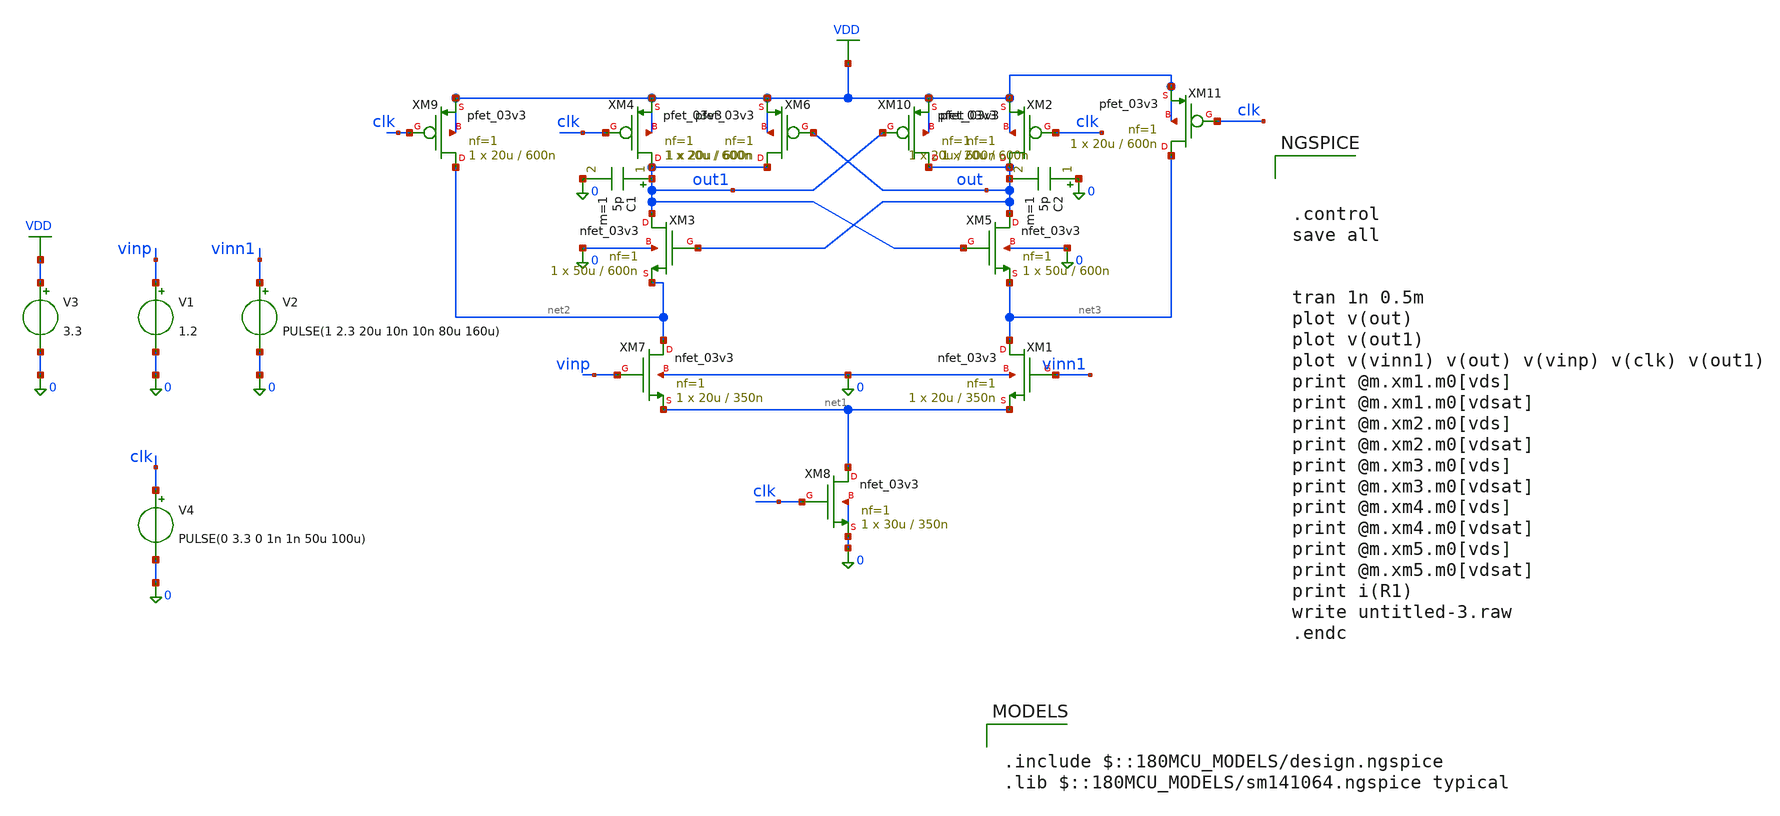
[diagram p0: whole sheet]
** sch_path: amplifier/untitled-3.sch
**.subckt untitled-3
XM4 out1 clk VDD VDD pfet_03v3 L=600n W=20u nf=1 ad='int((nf+1)/2) * W/nf * 0.18u' as='int((nf+2)/2) * W/nf * 0.18u'
+ pd='2*int((nf+1)/2) * (W/nf + 0.18u)' ps='2*int((nf+2)/2) * (W/nf + 0.18u)' nrd='0.18u / W' nrs='0.18u / W'
+ sa=0 sb=0 sd=0 m=1
V1 vinp 0 1.2
V2 vinn1 0 PULSE(1 2.3 20u 10n 10n 80u 160u)
V3 VDD 0 3.3
XM2 out clk VDD VDD pfet_03v3 L=600n W=20u nf=1 ad='int((nf+1)/2) * W/nf * 0.18u' as='int((nf+2)/2) * W/nf * 0.18u'
+ pd='2*int((nf+1)/2) * (W/nf + 0.18u)' ps='2*int((nf+2)/2) * (W/nf + 0.18u)' nrd='0.18u / W' nrs='0.18u / W'
+ sa=0 sb=0 sd=0 m=1
XM7 net2 vinp net1 0 nfet_03v3 L=350n W=20u nf=1 ad='int((nf+1)/2) * W/nf * 0.18u' as='int((nf+2)/2) * W/nf * 0.18u'
+ pd='2*int((nf+1)/2) * (W/nf + 0.18u)' ps='2*int((nf+2)/2) * (W/nf + 0.18u)' nrd='0.18u / W' nrs='0.18u / W'
+ sa=0 sb=0 sd=0 m=1
XM8 net1 clk 0 0 nfet_03v3 L=350n W=30u nf=1 ad='int((nf+1)/2) * W/nf * 0.18u' as='int((nf+2)/2) * W/nf * 0.18u'
+ pd='2*int((nf+1)/2) * (W/nf + 0.18u)' ps='2*int((nf+2)/2) * (W/nf + 0.18u)' nrd='0.18u / W' nrs='0.18u / W'
+ sa=0 sb=0 sd=0 m=1
XM1 net3 vinn1 net1 0 nfet_03v3 L=350n W=20u nf=1 ad='int((nf+1)/2) * W/nf * 0.18u' as='int((nf+2)/2) * W/nf * 0.18u'
+ pd='2*int((nf+1)/2) * (W/nf + 0.18u)' ps='2*int((nf+2)/2) * (W/nf + 0.18u)' nrd='0.18u / W' nrs='0.18u / W'
+ sa=0 sb=0 sd=0 m=1
XM3 out1 out net2 0 nfet_03v3 L=600n W=50u nf=1 ad='int((nf+1)/2) * W/nf * 0.18u' as='int((nf+2)/2) * W/nf * 0.18u'
+ pd='2*int((nf+1)/2) * (W/nf + 0.18u)' ps='2*int((nf+2)/2) * (W/nf + 0.18u)' nrd='0.18u / W' nrs='0.18u / W'
+ sa=0 sb=0 sd=0 m=1
XM5 out out1 net3 0 nfet_03v3 L=600n W=50u nf=1 ad='int((nf+1)/2) * W/nf * 0.18u' as='int((nf+2)/2) * W/nf * 0.18u'
+ pd='2*int((nf+1)/2) * (W/nf + 0.18u)' ps='2*int((nf+2)/2) * (W/nf + 0.18u)' nrd='0.18u / W' nrs='0.18u / W'
+ sa=0 sb=0 sd=0 m=1
V4 clk 0 PULSE(0 3.3 0 1n 1n 50u 100u)
XM6 out1 out VDD VDD pfet_03v3 L=600n W=20u nf=1 ad='int((nf+1)/2) * W/nf * 0.18u' as='int((nf+2)/2) * W/nf * 0.18u'
+ pd='2*int((nf+1)/2) * (W/nf + 0.18u)' ps='2*int((nf+2)/2) * (W/nf + 0.18u)' nrd='0.18u / W' nrs='0.18u / W'
+ sa=0 sb=0 sd=0 m=1
XM10 out out1 VDD VDD pfet_03v3 L=600n W=20u nf=1 ad='int((nf+1)/2) * W/nf * 0.18u' as='int((nf+2)/2) * W/nf * 0.18u'
+ pd='2*int((nf+1)/2) * (W/nf + 0.18u)' ps='2*int((nf+2)/2) * (W/nf + 0.18u)' nrd='0.18u / W' nrs='0.18u / W'
+ sa=0 sb=0 sd=0 m=1
XM9 net2 clk VDD VDD pfet_03v3 L=600n W=20u nf=1 ad='int((nf+1)/2) * W/nf * 0.18u' as='int((nf+2)/2) * W/nf * 0.18u'
+ pd='2*int((nf+1)/2) * (W/nf + 0.18u)' ps='2*int((nf+2)/2) * (W/nf + 0.18u)' nrd='0.18u / W' nrs='0.18u / W'
+ sa=0 sb=0 sd=0 m=1
XM11 net3 clk VDD VDD pfet_03v3 L=600n W=20u nf=1 ad='int((nf+1)/2) * W/nf * 0.18u' as='int((nf+2)/2) * W/nf * 0.18u'
+ pd='2*int((nf+1)/2) * (W/nf + 0.18u)' ps='2*int((nf+2)/2) * (W/nf + 0.18u)' nrd='0.18u / W' nrs='0.18u / W'
+ sa=0 sb=0 sd=0 m=1
C2 0 out 5p m=1
C1 out1 0 5p m=1
**** begin user architecture code

.include $::180MCU_MODELS/design.ngspice
.lib $::180MCU_MODELS/sm141064.ngspice typical




.control
save all


tran 1n 0.5m
plot v(out)
plot v(out1)
plot v(vinn1) v(out) v(vinp) v(clk) v(out1)
print @m.xm1.m0[vds]
print @m.xm1.m0[vdsat]
print @m.xm2.m0[vds]
print @m.xm2.m0[vdsat]
print @m.xm3.m0[vds]
print @m.xm3.m0[vdsat]
print @m.xm4.m0[vds]
print @m.xm4.m0[vdsat]
print @m.xm5.m0[vds]
print @m.xm5.m0[vdsat]
print i(R1)
write untitled-3.raw
.endc


**** end user architecture code
**.ends
.GLOBAL VDD
.end
